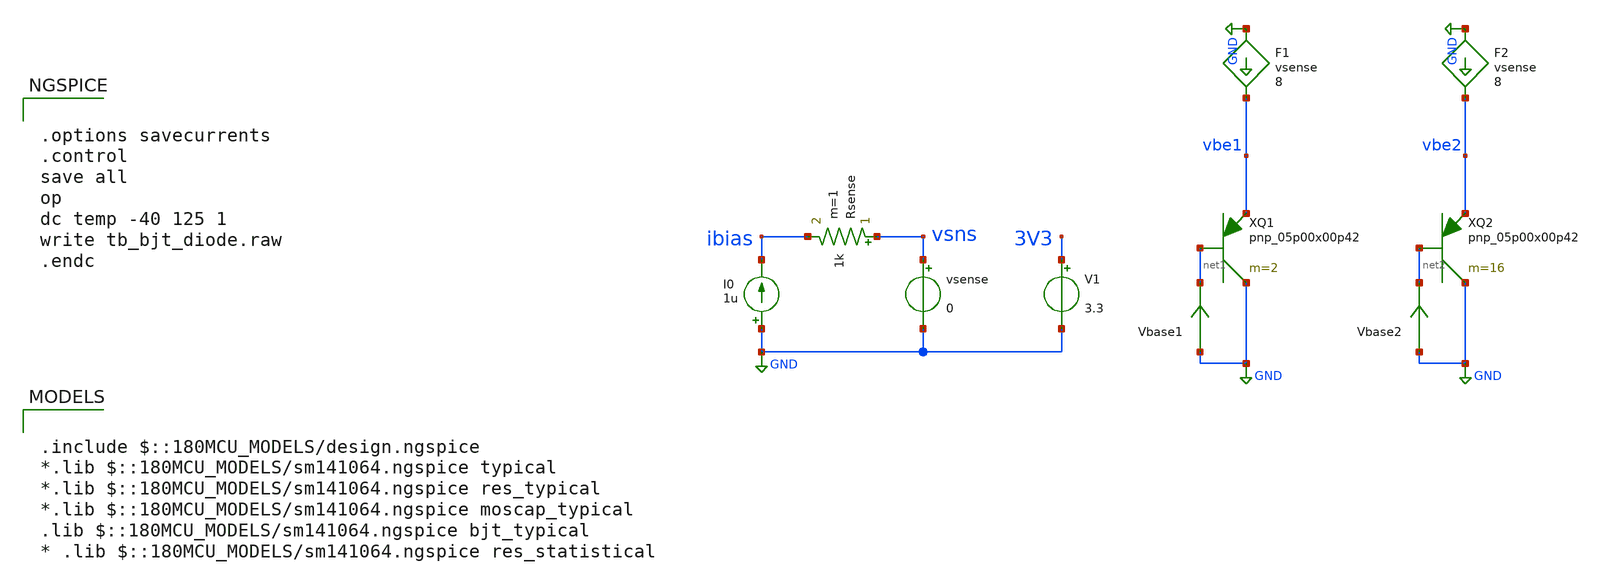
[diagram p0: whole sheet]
** sch_path: designs/libs/tb_analog/tb_bjt_diode/tb_bjt_diode.sch
**.subckt tb_bjt_diode
XQ1 GND net1 vbe1 pnp_05p00x00p42 m=2 par=2
I0 GND ibias 1u
Rsense vsns ibias 1k m=1
vsense vsns GND 0
V1 3V3 GND 3.3
F1 GND vbe1 vsense 8
F2 GND vbe2 vsense 8
XQ2 GND net2 vbe2 pnp_05p00x00p42 m=16 par=16
Vbase1 GND net1 0
.save i(vbase1)
Vbase2 GND net2 0
.save i(vbase2)
**** begin user architecture code

.include $::180MCU_MODELS/design.ngspice
*.lib $::180MCU_MODELS/sm141064.ngspice typical
*.lib $::180MCU_MODELS/sm141064.ngspice res_typical
*.lib $::180MCU_MODELS/sm141064.ngspice moscap_typical
.lib $::180MCU_MODELS/sm141064.ngspice bjt_typical
* .lib $::180MCU_MODELS/sm141064.ngspice res_statistical



.options savecurrents
.control
save all
op
dc temp -40 125 1
write tb_bjt_diode.raw
.endc


**** end user architecture code
**.ends
.GLOBAL GND
.end
